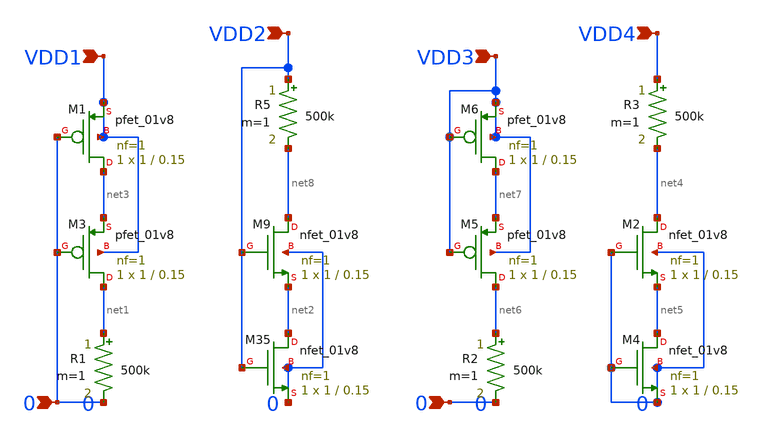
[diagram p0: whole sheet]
** sch_path: design/LELO_SVOD_SKY130A/TRANSISTOR_TEST.sch
**.subckt TRANSISTOR_TEST VDD1 VDD2 0 VDD4 VDD3 0
*.ipin VDD1
*.ipin VDD2
*.ipin 0
*.ipin VDD4
*.ipin VDD3
*.ipin 0
XM9 net8 VDD2 net2 0 sky130_fd_pr__nfet_01v8 L=0.15 W=1 nf=1 ad='int((1 + 1)/2) * 1 / 1 * 0.29' as='int((1 + 2)/2) * 1 / 1 * 0.29'
+ pd='2*int((1 + 1)/2) * (1 / 1 + 0.29)' ps='2*int((1 + 2)/2) * (1 / 1 + 0.29)' nrd='0.29 / 1 ' nrs='0.29 / 1 '
+ sa=0 sb=0 sd=0 mult=1 m=1
R5 VDD2 net8 500k m=1
XM35 net2 VDD2 0 0 sky130_fd_pr__nfet_01v8 L=0.15 W=1 nf=1 ad='int((1 + 1)/2) * 1 / 1 * 0.29' as='int((1 + 2)/2) * 1 / 1 * 0.29'
+ pd='2*int((1 + 1)/2) * (1 / 1 + 0.29)' ps='2*int((1 + 2)/2) * (1 / 1 + 0.29)' nrd='0.29 / 1 ' nrs='0.29 / 1 '
+ sa=0 sb=0 sd=0 mult=1 m=1
XM2 net4 0 net5 0 sky130_fd_pr__nfet_01v8 L=0.15 W=1 nf=1 ad='int((1 + 1)/2) * 1 / 1 * 0.29' as='int((1 + 2)/2) * 1 / 1 * 0.29'
+ pd='2*int((1 + 1)/2) * (1 / 1 + 0.29)' ps='2*int((1 + 2)/2) * (1 / 1 + 0.29)' nrd='0.29 / 1 ' nrs='0.29 / 1 '
+ sa=0 sb=0 sd=0 mult=1 m=1
XM5 net6 VDD3 net7 VDD3 sky130_fd_pr__pfet_01v8 L=0.15 W=1 nf=1 ad='int((1 + 1)/2) * 1 / 1 * 0.29' as='int((1 + 2)/2) * 1 / 1 * 0.29'
+ pd='2*int((1 + 1)/2) * (1 / 1 + 0.29)' ps='2*int((1 + 2)/2) * (1 / 1 + 0.29)' nrd='0.29 / 1 ' nrs='0.29 / 1 '
+ sa=0 sb=0 sd=0 mult=1 m=1
XM6 net7 VDD3 VDD3 VDD3 sky130_fd_pr__pfet_01v8 L=0.15 W=1 nf=1 ad='int((1 + 1)/2) * 1 / 1 * 0.29' as='int((1 + 2)/2) * 1 / 1 * 0.29'
+ pd='2*int((1 + 1)/2) * (1 / 1 + 0.29)' ps='2*int((1 + 2)/2) * (1 / 1 + 0.29)' nrd='0.29 / 1 ' nrs='0.29 / 1 '
+ sa=0 sb=0 sd=0 mult=1 m=1
R1 net1 0 500k m=1
R2 net6 0 500k m=1
R3 VDD4 net4 500k m=1
XM1 net3 0 VDD1 VDD1 sky130_fd_pr__pfet_01v8 L=0.15 W=1 nf=1 ad='int((1 + 1)/2) * 1 / 1 * 0.29' as='int((1 + 2)/2) * 1 / 1 * 0.29'
+ pd='2*int((1 + 1)/2) * (1 / 1 + 0.29)' ps='2*int((1 + 2)/2) * (1 / 1 + 0.29)' nrd='0.29 / 1 ' nrs='0.29 / 1 '
+ sa=0 sb=0 sd=0 mult=1 m=1
XM3 net1 0 net3 VDD1 sky130_fd_pr__pfet_01v8 L=0.15 W=1 nf=1 ad='int((1 + 1)/2) * 1 / 1 * 0.29' as='int((1 + 2)/2) * 1 / 1 * 0.29'
+ pd='2*int((1 + 1)/2) * (1 / 1 + 0.29)' ps='2*int((1 + 2)/2) * (1 / 1 + 0.29)' nrd='0.29 / 1 ' nrs='0.29 / 1 '
+ sa=0 sb=0 sd=0 mult=1 m=1
XM4 net5 0 0 0 sky130_fd_pr__nfet_01v8 L=0.15 W=1 nf=1 ad='int((1 + 1)/2) * 1 / 1 * 0.29' as='int((1 + 2)/2) * 1 / 1 * 0.29'
+ pd='2*int((1 + 1)/2) * (1 / 1 + 0.29)' ps='2*int((1 + 2)/2) * (1 / 1 + 0.29)' nrd='0.29 / 1 ' nrs='0.29 / 1 '
+ sa=0 sb=0 sd=0 mult=1 m=1
**.ends
.end
